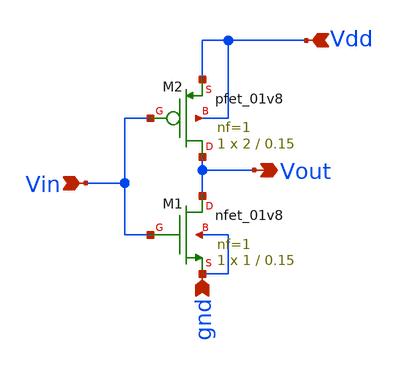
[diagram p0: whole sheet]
** sch_path: schematics/CMOS_inverter.sch
**.subckt CMOS_inverter Vin Vdd Vout gnd
*.ipin Vin
*.ipin Vdd
*.opin Vout
*.ipin gnd
XM1 Vout Vin gnd gnd sky130_fd_pr__nfet_01v8 L=0.15 W=1 nf=1 ad='int((1 + 1)/2) * 1 / 1 * 0.29' as='int((1 + 2)/2) * 1 / 1 * 0.29'
+ pd='2*int((1 + 1)/2) * (1 / 1 + 0.29)' ps='2*int((1 + 2)/2) * (1 / 1 + 0.29)' nrd='0.29 / 1 ' nrs='0.29 / 1 '
+ sa=0 sb=0 sd=0 mult=1 m=1
XM2 Vout Vin Vdd Vdd sky130_fd_pr__pfet_01v8 L=0.15 W=2 nf=1 ad='int((1 + 1)/2) * 2 / 1 * 0.29' as='int((1 + 2)/2) * 2 / 1 * 0.29'
+ pd='2*int((1 + 1)/2) * (2 / 1 + 0.29)' ps='2*int((1 + 2)/2) * (2 / 1 + 0.29)' nrd='0.29 / 2 ' nrs='0.29 / 2 '
+ sa=0 sb=0 sd=0 mult=1 m=1
**.ends
.end
